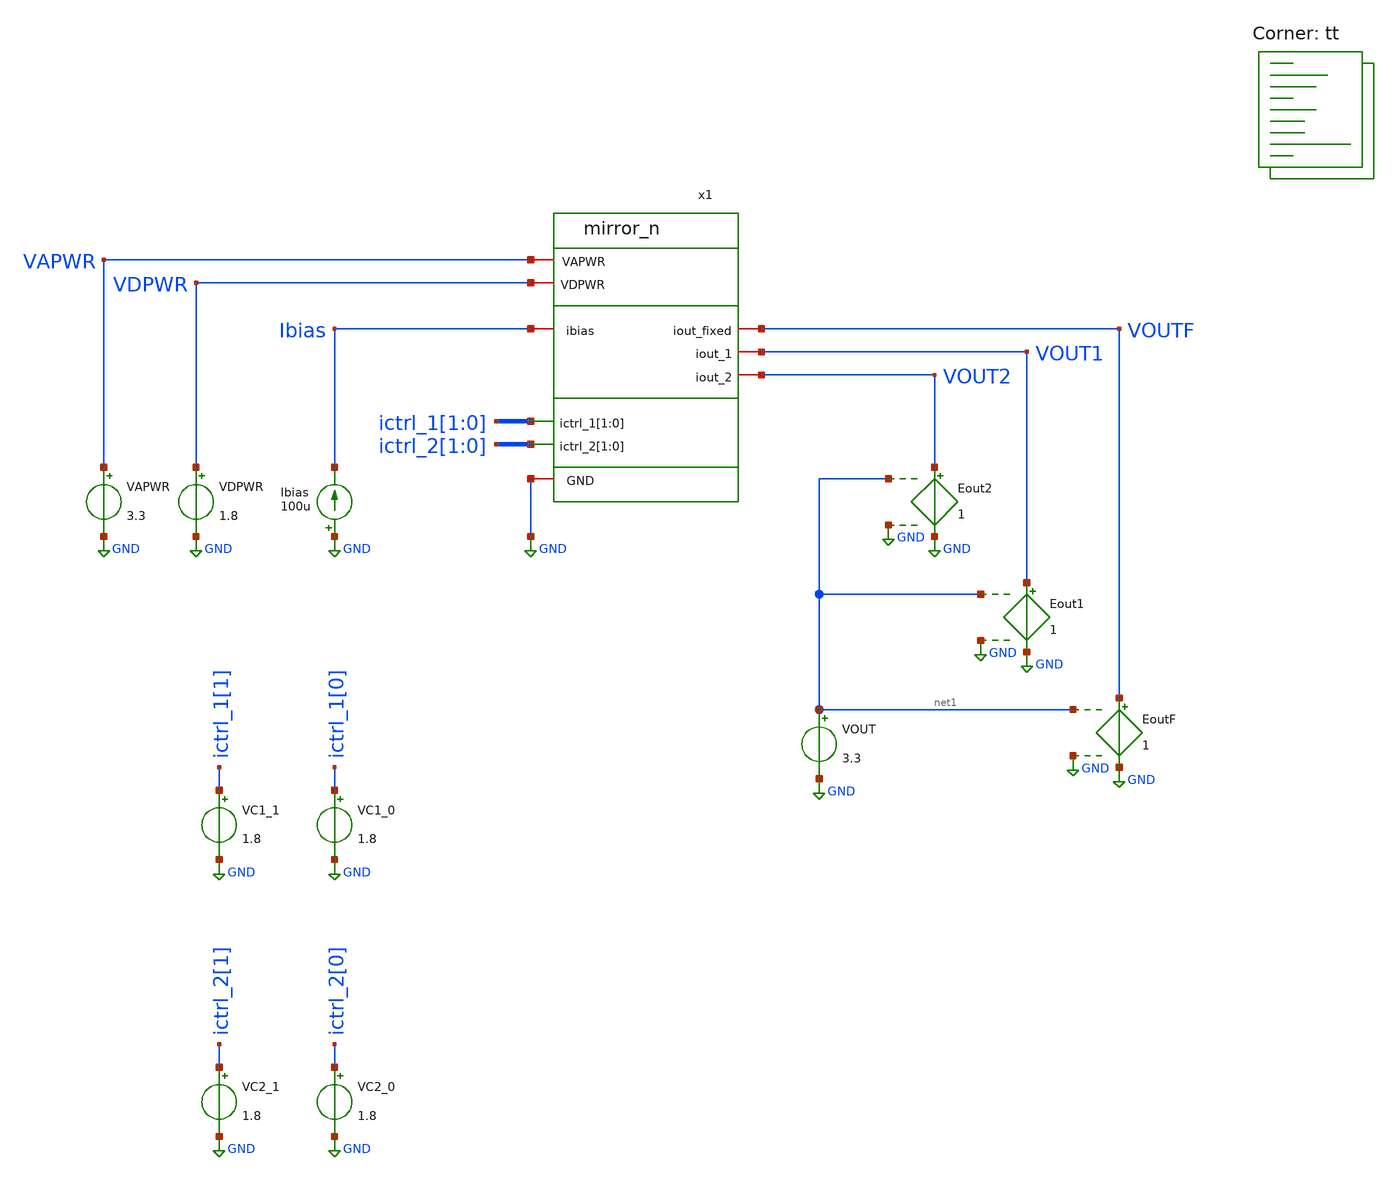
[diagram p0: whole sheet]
** sch_path: xschem/tb_mirror_n.sch
**.subckt tb_mirror_n
x1 VAPWR VDPWR Ibias VOUTF VOUT1 VOUT2 ictrl_1[1] ictrl_1[0] ictrl_2[1] ictrl_2[0] GND mirror_n
VAPWR VAPWR GND 3.3
VDPWR VDPWR GND 1.8
Ibias GND Ibias 100u
VOUT net1 GND 3.3
VC1_1 ictrl_1[1] GND 1.8
VC1_0 ictrl_1[0] GND 1.8
VC2_1 ictrl_2[1] GND 1.8
VC2_0 ictrl_2[0] GND 1.8
Eout2 VOUT2 GND net1 GND 1
Eout1 VOUT1 GND net1 GND 1
EoutF VOUTF GND net1 GND 1
**** begin user architecture code
.lib $::SKYWATER_MODELS/sky130.lib.spice tt


*****************************************
* Vout DC Sweep Test
*****************************************
* With a fixed input current, sweeps the output voltage
* and plots the output voltage for (1) programmable mirror 1 across codes
* (2) programmable mirror 2 across codes (3) programmable mirror 1 vs fixed output
*****************************************
.control
   save all
   alter vc1_1 0
   alter vc1_0 0
   alter vc2_1 0
   alter vc2_0 0
   set temp = 27
   set wr_singlescale
   set wr_vecnames
   set output_str = 'tb_mirror_n.raw' ; dont change this. handled in python
   * the below 3x nested loop is required to step ctrl[1:0] from 0 to 3
   * control for idac1 and idac2 are swept together
   repeat 2
      repeat 2
         dc Vout 0 3.3 0.01
         alter vc1_0 1.8
         alter vc2_0 1.8
      end
      alter vc1_1 1.8
      alter vc1_0 0
      alter vc2_1 1.8
      alter vc2_0 0
   end
   plot (-dc1.i(eout1)) (-dc2.i(eout1)) (-dc3.i(eout1)) (-dc4.i(eout1)) ; output current of idac1
   plot (-dc1.i(eout2)) (-dc2.i(eout2)) (-dc3.i(eout2)) (-dc4.i(eout2)); output current of idac2
   plot (-dc1.i(eout1)) (-dc2.i(eoutf)) ; comparing transmission gate output vs ungated output

*   wrdata $output_str (-dc1.i(eout1)) (-dc2.i(eout1)) (-dc3.i(eout1)) (-dc4.i(eout1))
*+ (-dc1.i(eoutf)) (-dc1.i(eout2)) (-dc2.i(eout2)) (-dc3.i(eout2)) (-dc4.i(eout2))
.endc


**** end user architecture code
**.ends
.GLOBAL GND
.end
